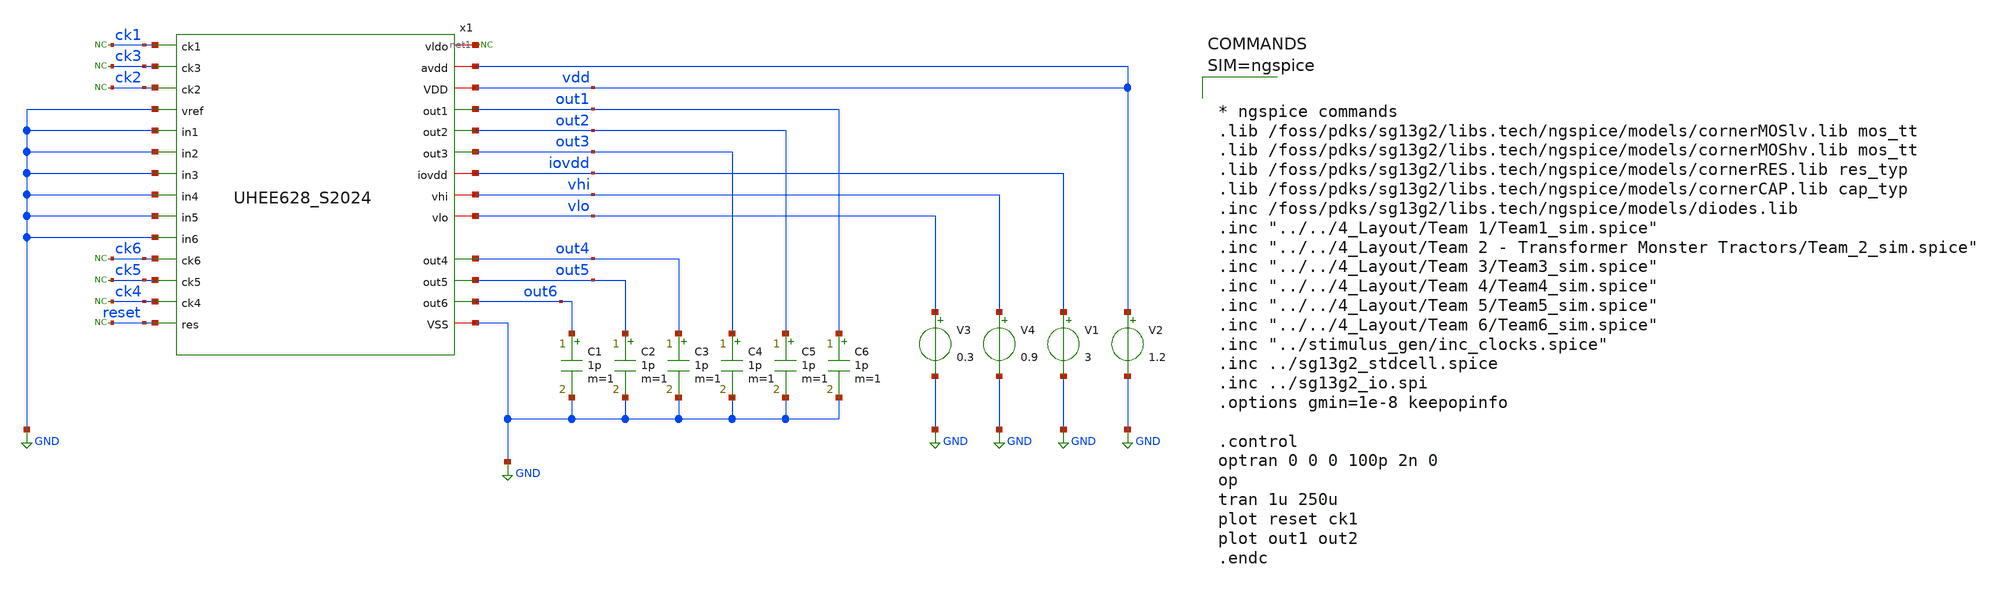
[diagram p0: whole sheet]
** sch_path: 5_Design/3_Real_circuits/tb_UHEE628_S2024.sch
**.subckt tb_UHEE628_S2024
x1 net1 ck1 ck3 vdd ck2 vdd GND out1 GND GND out2 out3 GND iovdd vhi vlo out4 GND out5 GND out6 GND
+ ck6 ck5 ck4 reset GND UHEE628_S2024
V1 iovdd GND 3
V2 vdd GND 1.2
* noconn #net1
V3 vlo GND 0.3
V4 vhi GND 0.9
C1 out6 GND 1p m=1
C2 out5 GND 1p m=1
C3 out4 GND 1p m=1
C4 out3 GND 1p m=1
C5 out2 GND 1p m=1
C6 out1 GND 1p m=1
* noconn ck1
* noconn ck3
* noconn ck2
* noconn ck6
* noconn ck5
* noconn ck4
* noconn reset
**** begin user architecture code



* ngspice commands
.lib /foss/pdks/sg13g2/libs.tech/ngspice/models/cornerMOSlv.lib mos_tt
.lib /foss/pdks/sg13g2/libs.tech/ngspice/models/cornerMOShv.lib mos_tt
.lib /foss/pdks/sg13g2/libs.tech/ngspice/models/cornerRES.lib res_typ
.lib /foss/pdks/sg13g2/libs.tech/ngspice/models/cornerCAP.lib cap_typ
.inc /foss/pdks/sg13g2/libs.tech/ngspice/models/diodes.lib
.inc "../../4_Layout/Team 1/Team1_sim.spice"
.inc "../../4_Layout/Team 2 - Transformer Monster Tractors/Team_2_sim.spice"
.inc "../../4_Layout/Team 3/Team3_sim.spice"
.inc "../../4_Layout/Team 4/Team4_sim.spice"
.inc "../../4_Layout/Team 5/Team5_sim.spice"
.inc "../../4_Layout/Team 6/Team6_sim.spice"
.inc "../stimulus_gen/inc_clocks.spice"
.inc ../sg13g2_stdcell.spice
.inc ../sg13g2_io.spi
.options gmin=1e-8 keepopinfo

.control
optran 0 0 0 100p 2n 0
op
tran 1u 250u
plot reset ck1
plot out1 out2
.endc


**** end user architecture code
**.ends
.GLOBAL GND
.end
